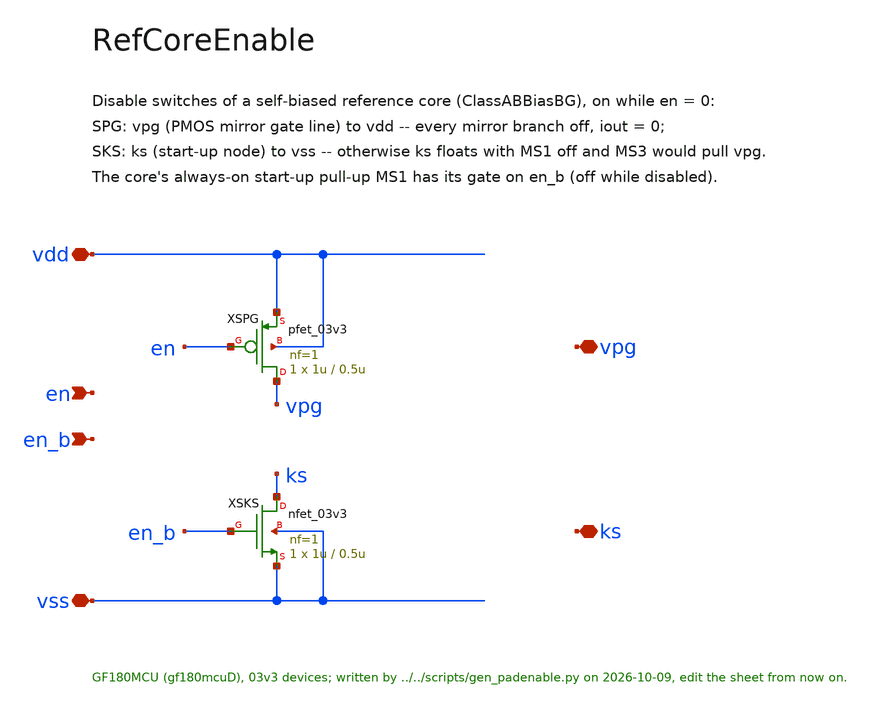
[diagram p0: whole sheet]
** sch_path: macros/PadEnable/schematic/xschem/RefCoreEnable.sch
**.subckt RefCoreEnable vdd vss en en_b vpg ks
*.iopin vdd
*.iopin vss
*.ipin en
*.ipin en_b
*.iopin vpg
*.iopin ks
XSPG vpg en vdd vdd pfet_03v3 L=0.5u W=1u nf=1 ad='int((nf+1)/2) * W/nf * 0.18u' as='int((nf+2)/2) * W/nf * 0.18u'
+ pd='2*int((nf+1)/2) * (W/nf + 0.18u)' ps='2*int((nf+2)/2) * (W/nf + 0.18u)' nrd='0.18u / W' nrs='0.18u / W'
+ sa=0 sb=0 sd=0 m=1
XSKS ks en_b vss vss nfet_03v3 L=0.5u W=1u nf=1 ad='int((nf+1)/2) * W/nf * 0.18u' as='int((nf+2)/2) * W/nf * 0.18u'
+ pd='2*int((nf+1)/2) * (W/nf + 0.18u)' ps='2*int((nf+2)/2) * (W/nf + 0.18u)' nrd='0.18u / W' nrs='0.18u / W'
+ sa=0 sb=0 sd=0 m=1
**.ends
.end
